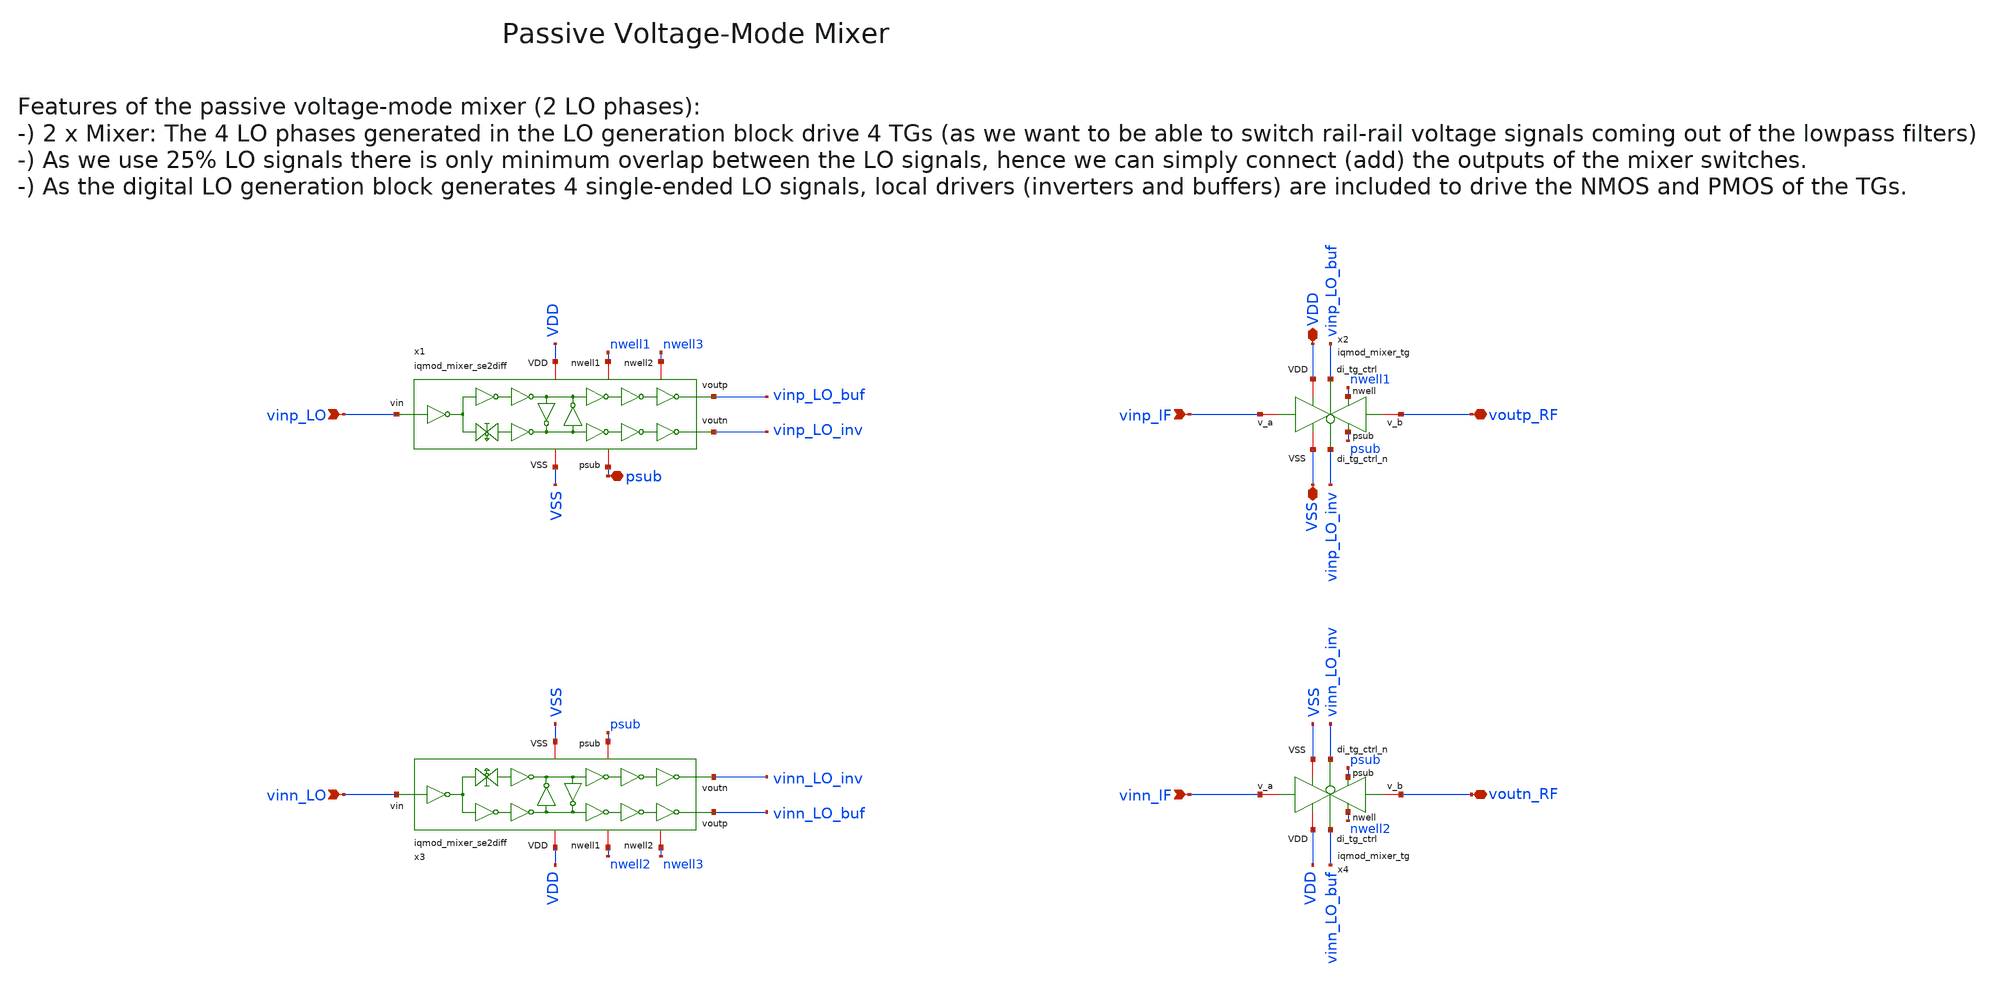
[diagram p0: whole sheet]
** sch_path: ihp130/macros/iqmod/xschem/iqmod_mixer.sch
**.subckt iqmod_mixer VDD VSS vinp_IF vinn_IF voutp_RF vinp_LO vinn_LO voutn_RF psub
*.iopin VDD
*.iopin VSS
*.ipin vinp_IF
*.ipin vinn_IF
*.iopin voutp_RF
*.ipin vinp_LO
*.ipin vinn_LO
*.iopin voutn_RF
*.iopin psub
x2 nwell1 psub VDD vinp_LO_buf VSS voutp_RF vinp_IF vinp_LO_inv iqmod_mixer_tg
x4 nwell2 psub VDD vinn_LO_buf VSS voutn_RF vinn_IF vinn_LO_inv iqmod_mixer_tg
x1 nwell1 psub nwell3 VDD vinp_LO vinp_LO_buf VSS vinp_LO_inv iqmod_mixer_se2diff
x3 nwell2 psub nwell3 VDD vinn_LO vinn_LO_buf VSS vinn_LO_inv iqmod_mixer_se2diff
**.ends
.end
